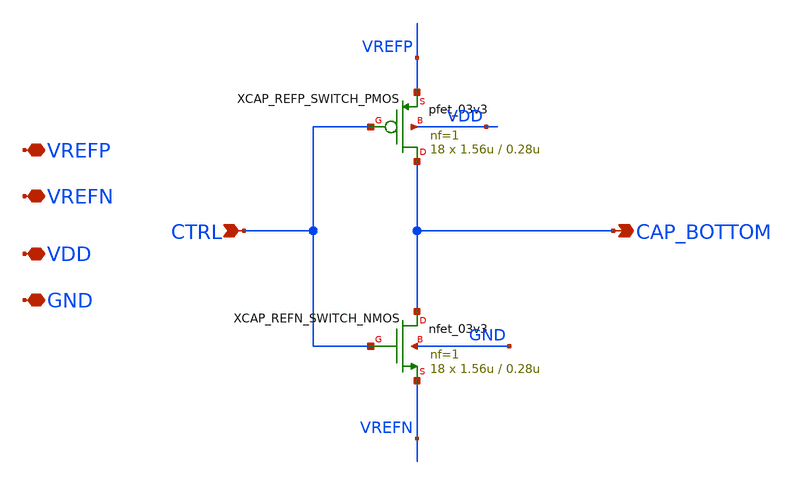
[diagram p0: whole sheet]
** sch_path: verification/a44_w5p29_trans_driver/01_CURRENT_CIRCUIT_FILES/xschem/A44_CAP_SWITCH.sch
**.subckt A44_CAP_SWITCH VREFP VREFN CTRL CAP_BOTTOM VDD GND
*.iopin VREFP
*.iopin VREFN
*.ipin CTRL
*.opin CAP_BOTTOM
*.iopin VDD
*.iopin GND
XCAP_REFN_SWITCH_NMOS CAP_BOTTOM CTRL VREFN GND nfet_03v3 L=0.28u W=1.56u nf=1 ad='int((nf+1)/2) * W/nf * 0.18u'
+ as='int((nf+2)/2) * W/nf * 0.18u' pd='2*int((nf+1)/2) * (W/nf + 0.18u)' ps='2*int((nf+2)/2) * (W/nf + 0.18u)'
+ nrd='0.18u / W' nrs='0.18u / W' sa=0 sb=0 sd=0 m=18
XCAP_REFP_SWITCH_PMOS CAP_BOTTOM CTRL VREFP VDD pfet_03v3 L=0.28u W=1.56u nf=1 ad='int((nf+1)/2) * W/nf * 0.18u'
+ as='int((nf+2)/2) * W/nf * 0.18u' pd='2*int((nf+1)/2) * (W/nf + 0.18u)' ps='2*int((nf+2)/2) * (W/nf + 0.18u)'
+ nrd='0.18u / W' nrs='0.18u / W' sa=0 sb=0 sd=0 m=18
**.ends
.end
